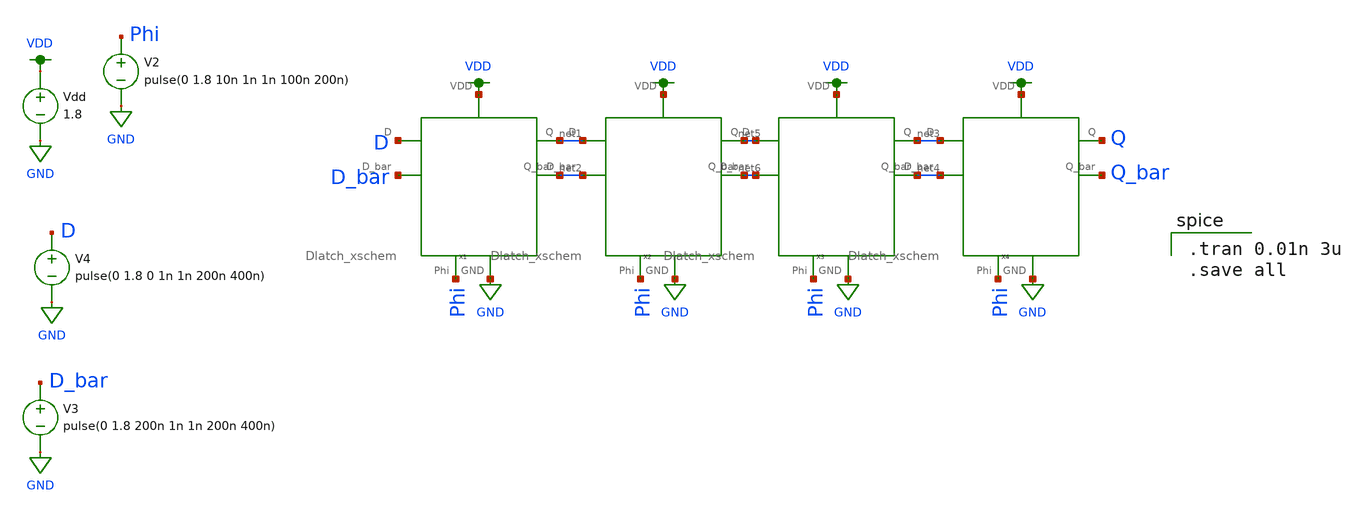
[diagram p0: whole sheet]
** sch_path: Homework2/Shift_Register_xschem.sch
**.subckt Shift_Register_xschem
Vdd VDD GND 1.8
V2 Phi GND pulse(0 1.8 10n 1n 1n 100n 200n)
V3 D_bar GND pulse(0 1.8 200n 1n 1n 200n 400n)
V4 D GND pulse(0 1.8 0 1n 1n 200n 400n)
X1 D D_bar VDD net1 net2 GND Phi Dlatch_xschem
X2 net1 net2 VDD net5 net6 GND Phi Dlatch_xschem
X3 net5 net6 VDD net3 net4 GND Phi Dlatch_xschem
X4 net3 net4 VDD Q Q_bar GND Phi Dlatch_xschem
**** begin user architecture code

.option wnflag=1
.lib ~/skywater/skywater-pdk/libraries/sky130_fd_pr_ngspice/latest/models/sky130.lib.spice tt


.tran 0.01n 3u
.save all

**** end user architecture code
**.ends

* expanding   symbol:  /home/madvlsi/Documents/MADVLSI/Homework2/Dlatch_xschem.sym # of pins=7
** sym_path: Homework2/Dlatch_xschem.sym
** sch_path: Homework2/Dlatch_xschem.sch
.subckt Dlatch_xschem D D_bar VDD Q Q_bar GND Phi
*.iopin VDD
*.iopin GND
*.ipin D
*.ipin D_bar
*.ipin Phi
*.opin Q
*.opin Q_bar
XM1 net1 Phi Q GND sky130_fd_pr__nfet_01v8 L=0.15 W=1 nf=1 ad='int((nf+1)/2) * W/nf * 0.29' as='int((nf+2)/2) * W/nf * 0.29'
+ pd='2*int((nf+1)/2) * (W/nf + 0.29)' ps='2*int((nf+2)/2) * (W/nf + 0.29)' nrd='0.29 / W' nrs='0.29 / W'
+ sa=0 sb=0 sd=0 mult=1 m=1
XM2 net2 Phi Q_bar GND sky130_fd_pr__nfet_01v8 L=0.15 W=1 nf=1 ad='int((nf+1)/2) * W/nf * 0.29' as='int((nf+2)/2) * W/nf * 0.29'
+ pd='2*int((nf+1)/2) * (W/nf + 0.29)' ps='2*int((nf+2)/2) * (W/nf + 0.29)' nrd='0.29 / W' nrs='0.29 / W'
+ sa=0 sb=0 sd=0 mult=1 m=1
XM3 GND Q_bar Q GND sky130_fd_pr__nfet_01v8 L=0.15 W=1 nf=1 ad='int((nf+1)/2) * W/nf * 0.29' as='int((nf+2)/2) * W/nf * 0.29'
+ pd='2*int((nf+1)/2) * (W/nf + 0.29)' ps='2*int((nf+2)/2) * (W/nf + 0.29)' nrd='0.29 / W' nrs='0.29 / W'
+ sa=0 sb=0 sd=0 mult=1 m=1
XM4 Q_bar Q GND GND sky130_fd_pr__nfet_01v8 L=0.15 W=1 nf=1 ad='int((nf+1)/2) * W/nf * 0.29' as='int((nf+2)/2) * W/nf * 0.29'
+ pd='2*int((nf+1)/2) * (W/nf + 0.29)' ps='2*int((nf+2)/2) * (W/nf + 0.29)' nrd='0.29 / W' nrs='0.29 / W'
+ sa=0 sb=0 sd=0 mult=1 m=1
XM5 net4 Q_bar Q VDD sky130_fd_pr__pfet_01v8 L=0.15 W=1 nf=1 ad='int((nf+1)/2) * W/nf * 0.29' as='int((nf+2)/2) * W/nf * 0.29'
+ pd='2*int((nf+1)/2) * (W/nf + 0.29)' ps='2*int((nf+2)/2) * (W/nf + 0.29)' nrd='0.29 / W' nrs='0.29 / W'
+ sa=0 sb=0 sd=0 mult=1 m=1
XM7 Q_bar Q net4 VDD sky130_fd_pr__pfet_01v8 L=0.15 W=1 nf=1 ad='int((nf+1)/2) * W/nf * 0.29' as='int((nf+2)/2) * W/nf * 0.29'
+ pd='2*int((nf+1)/2) * (W/nf + 0.29)' ps='2*int((nf+2)/2) * (W/nf + 0.29)' nrd='0.29 / W' nrs='0.29 / W'
+ sa=0 sb=0 sd=0 mult=1 m=1
XM8 net4 Phi VDD VDD sky130_fd_pr__pfet_01v8 L=0.15 W=1 nf=1 ad='int((nf+1)/2) * W/nf * 0.29' as='int((nf+2)/2) * W/nf * 0.29'
+ pd='2*int((nf+1)/2) * (W/nf + 0.29)' ps='2*int((nf+2)/2) * (W/nf + 0.29)' nrd='0.29 / W' nrs='0.29 / W'
+ sa=0 sb=0 sd=0 mult=2 m=2
XM9 net1 Phi D VDD sky130_fd_pr__pfet_01v8 L=0.15 W=1 nf=1 ad='int((nf+1)/2) * W/nf * 0.29' as='int((nf+2)/2) * W/nf * 0.29'
+ pd='2*int((nf+1)/2) * (W/nf + 0.29)' ps='2*int((nf+2)/2) * (W/nf + 0.29)' nrd='0.29 / W' nrs='0.29 / W'
+ sa=0 sb=0 sd=0 mult=1 m=1
XM10 net2 Phi D_bar VDD sky130_fd_pr__pfet_01v8 L=0.15 W=1 nf=1 ad='int((nf+1)/2) * W/nf * 0.29' as='int((nf+2)/2) * W/nf * 0.29'
+ pd='2*int((nf+1)/2) * (W/nf + 0.29)' ps='2*int((nf+2)/2) * (W/nf + 0.29)' nrd='0.29 / W' nrs='0.29 / W'
+ sa=0 sb=0 sd=0 mult=1 m=1
XM11 VDD net1 net2 VDD sky130_fd_pr__pfet_01v8 L=0.15 W=1 nf=1 ad='int((nf+1)/2) * W/nf * 0.29' as='int((nf+2)/2) * W/nf * 0.29'
+ pd='2*int((nf+1)/2) * (W/nf + 0.29)' ps='2*int((nf+2)/2) * (W/nf + 0.29)' nrd='0.29 / W' nrs='0.29 / W'
+ sa=0 sb=0 sd=0 mult=1 m=1
XM12 net1 net2 VDD VDD sky130_fd_pr__pfet_01v8 L=0.15 W=1 nf=1 ad='int((nf+1)/2) * W/nf * 0.29' as='int((nf+2)/2) * W/nf * 0.29'
+ pd='2*int((nf+1)/2) * (W/nf + 0.29)' ps='2*int((nf+2)/2) * (W/nf + 0.29)' nrd='0.29 / W' nrs='0.29 / W'
+ sa=0 sb=0 sd=0 mult=1 m=1
XM13 net3 net1 net2 GND sky130_fd_pr__nfet_01v8 L=0.15 W=1 nf=1 ad='int((nf+1)/2) * W/nf * 0.29' as='int((nf+2)/2) * W/nf * 0.29'
+ pd='2*int((nf+1)/2) * (W/nf + 0.29)' ps='2*int((nf+2)/2) * (W/nf + 0.29)' nrd='0.29 / W' nrs='0.29 / W'
+ sa=0 sb=0 sd=0 mult=1 m=1
XM14 net1 net2 net3 GND sky130_fd_pr__nfet_01v8 L=0.15 W=1 nf=1 ad='int((nf+1)/2) * W/nf * 0.29' as='int((nf+2)/2) * W/nf * 0.29'
+ pd='2*int((nf+1)/2) * (W/nf + 0.29)' ps='2*int((nf+2)/2) * (W/nf + 0.29)' nrd='0.29 / W' nrs='0.29 / W'
+ sa=0 sb=0 sd=0 mult=1 m=1
XM15 net3 Phi GND GND sky130_fd_pr__nfet_01v8 L=0.15 W=1 nf=1 ad='int((nf+1)/2) * W/nf * 0.29' as='int((nf+2)/2) * W/nf * 0.29'
+ pd='2*int((nf+1)/2) * (W/nf + 0.29)' ps='2*int((nf+2)/2) * (W/nf + 0.29)' nrd='0.29 / W' nrs='0.29 / W'
+ sa=0 sb=0 sd=0 mult=2 m=2
.ends

.GLOBAL GND
.GLOBAL VDD
.end
